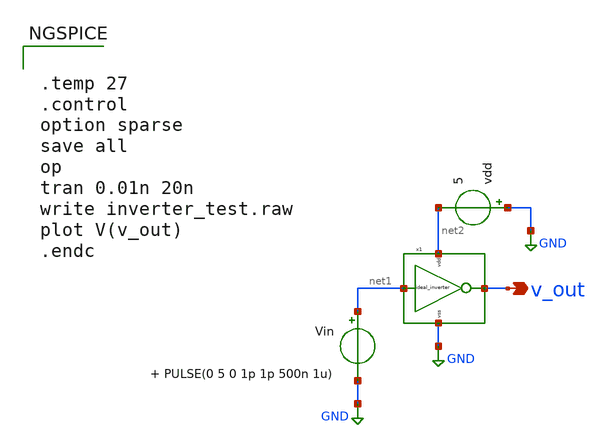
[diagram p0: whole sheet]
** sch_path: 2_ideal_circuits/ideal_inverter_tb.sch
**.subckt ideal_inverter_tb v_out
*.opin v_out
vdd GND net2 5
Vin net1 GND PULSE(0 5 0 1p 1p 500n 1u)

x1 v_out net1 GND net2 ideal_inverter
**** begin user architecture code


.temp 27
.control
option sparse
save all
op
tran 0.01n 20n
write inverter_test.raw
plot V(v_out)
.endc


**** end user architecture code
**.ends

* expanding   symbol:  ideal_inverter.sym # of pins=4
** sym_path: 2_ideal_circuits/ideal_inverter.sym
** sch_path: 2_ideal_circuits/ideal_inverter.sch
.subckt ideal_inverter out in vss vdd
*.iopin vdd
*.ipin in
*.opin out
*.iopin vss
B1 out GND V={v(in)>v(vdd)/2?v(vss):v(vdd)}
* noconn vdd
* noconn in
* noconn vss
.ends

.GLOBAL GND
.end
